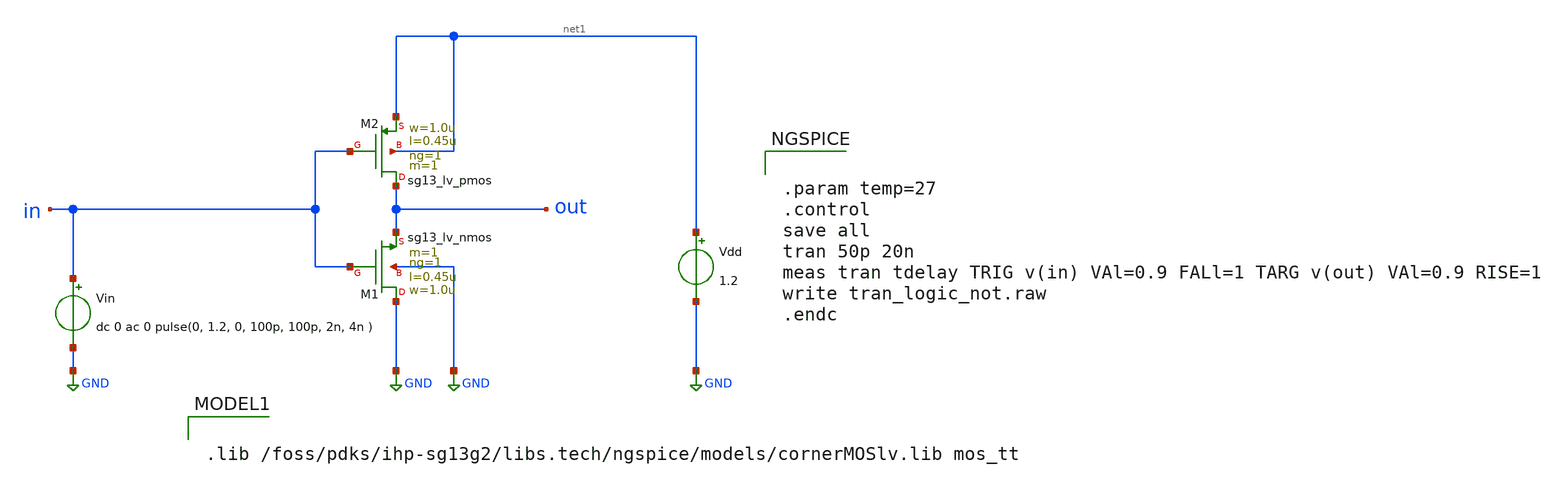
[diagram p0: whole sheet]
** sch_path: content/simulation_files/xschem/06_tran_logic_not.sch
* Copyright 2023 IHP PDK Authors
**.subckt 06_tran_logic_not
Vin in GND dc 0 ac 0 pulse(0, 1.2, 0, 100p, 100p, 2n, 4n )
Vdd net1 GND 1.2
XM1 GND in out GND sg13_lv_nmos w=1.0u l=0.45u ng=1 m=1 mm_ok=1
XM2 out in net1 net1 sg13_lv_pmos w=1.0u l=0.45u ng=1 m=1 mm_ok=1
**** begin user architecture code


.param temp=27
.control
save all
tran 50p 20n
meas tran tdelay TRIG v(in) VAl=0.9 FALl=1 TARG v(out) VAl=0.9 RISE=1
write tran_logic_not.raw
.endc



.lib /foss/pdks/ihp-sg13g2/libs.tech/ngspice/models/cornerMOSlv.lib mos_tt

**** end user architecture code
**.ends
.GLOBAL GND
.end
